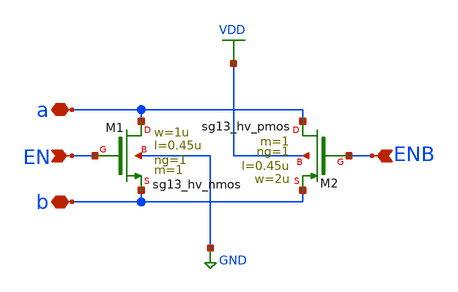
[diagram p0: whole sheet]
** sch_path: 3_real_circuits/tg_hv.sch
**.subckt tg_hv ENB EN b a
*.ipin ENB
*.ipin EN
*.iopin b
*.iopin a
XM2 a ENB b VDD sg13_hv_pmos w=2u l=0.45u ng=1 m=1 mm_ok=1
XM1 a EN b GND sg13_hv_nmos w=1u l=0.45u ng=1 m=1 mm_ok=1
**.ends
.GLOBAL VDD
.GLOBAL GND
.end
